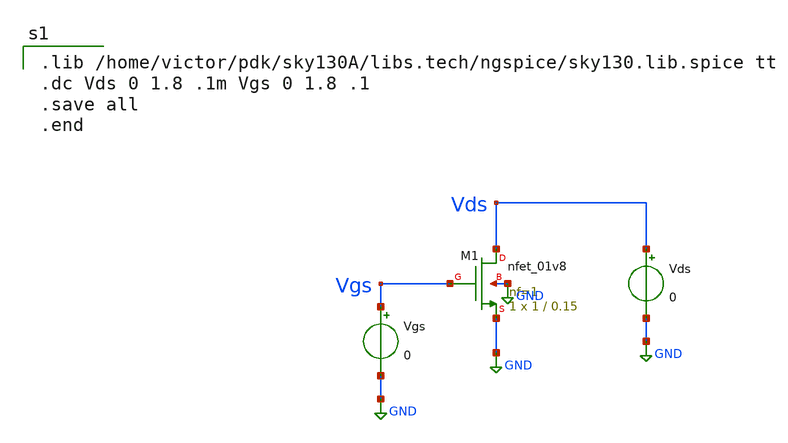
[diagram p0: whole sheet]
** sch_path: Schematics/NMOSIVCharacteristics.sch
**.subckt NMOSIVCharacteristics
XM1 Vds Vgs GND GND sky130_fd_pr__nfet_01v8 L=0.15 W=1 nf=1 ad='int((nf+1)/2) * W/nf * 0.29' as='int((nf+2)/2) * W/nf * 0.29'
+ pd='2*int((nf+1)/2) * (W/nf + 0.29)' ps='2*int((nf+2)/2) * (W/nf + 0.29)' nrd='0.29 / W' nrs='0.29 / W'
+ sa=0 sb=0 sd=0 mult=1 m=1
Vds Vds GND 0
Vgs Vgs GND 0
**** begin user architecture code

.lib /home/victor/pdk/sky130A/libs.tech/ngspice/sky130.lib.spice tt
.dc Vds 0 1.8 .1m Vgs 0 1.8 .1
.save all
.end

**** end user architecture code
**.ends
.GLOBAL GND
.end
